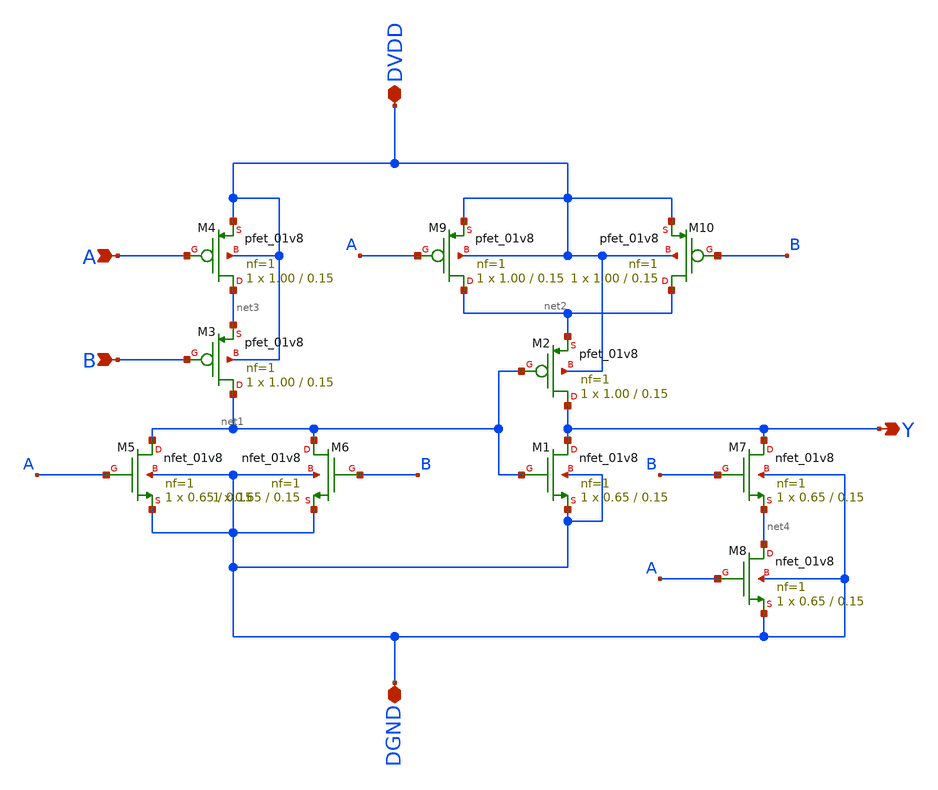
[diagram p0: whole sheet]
** sch_path: project/sch_sym_files/xor2.sch
**.subckt xor2 DVDD DGND A B Y
*.iopin DVDD
*.iopin DGND
*.ipin A
*.ipin B
*.opin Y
XM2 Y net1 net2 DVDD sky130_fd_pr__pfet_01v8 L=0.15 W=1.00 nf=1 ad='int((nf+1)/2) * W/nf * 0.29' as='int((nf+2)/2) * W/nf * 0.29'
+ pd='2*int((nf+1)/2) * (W/nf + 0.29)' ps='2*int((nf+2)/2) * (W/nf + 0.29)' nrd='0.29 / W' nrs='0.29 / W'
+ sa=0 sb=0 sd=0 mult=1 m=1
XM1 Y net1 DGND DGND sky130_fd_pr__nfet_01v8 L=0.15 W=0.65 nf=1 ad='int((nf+1)/2) * W/nf * 0.29' as='int((nf+2)/2) * W/nf * 0.29'
+ pd='2*int((nf+1)/2) * (W/nf + 0.29)' ps='2*int((nf+2)/2) * (W/nf + 0.29)' nrd='0.29 / W' nrs='0.29 / W'
+ sa=0 sb=0 sd=0 mult=1 m=1
XM3 net1 B net3 DVDD sky130_fd_pr__pfet_01v8 L=0.15 W=1.00 nf=1 ad='int((nf+1)/2) * W/nf * 0.29' as='int((nf+2)/2) * W/nf * 0.29'
+ pd='2*int((nf+1)/2) * (W/nf + 0.29)' ps='2*int((nf+2)/2) * (W/nf + 0.29)' nrd='0.29 / W' nrs='0.29 / W'
+ sa=0 sb=0 sd=0 mult=1 m=1
XM4 net3 A DVDD DVDD sky130_fd_pr__pfet_01v8 L=0.15 W=1.00 nf=1 ad='int((nf+1)/2) * W/nf * 0.29' as='int((nf+2)/2) * W/nf * 0.29'
+ pd='2*int((nf+1)/2) * (W/nf + 0.29)' ps='2*int((nf+2)/2) * (W/nf + 0.29)' nrd='0.29 / W' nrs='0.29 / W'
+ sa=0 sb=0 sd=0 mult=1 m=1
XM5 net1 A DGND DGND sky130_fd_pr__nfet_01v8 L=0.15 W=0.65 nf=1 ad='int((nf+1)/2) * W/nf * 0.29' as='int((nf+2)/2) * W/nf * 0.29'
+ pd='2*int((nf+1)/2) * (W/nf + 0.29)' ps='2*int((nf+2)/2) * (W/nf + 0.29)' nrd='0.29 / W' nrs='0.29 / W'
+ sa=0 sb=0 sd=0 mult=1 m=1
XM6 net1 B DGND DGND sky130_fd_pr__nfet_01v8 L=0.15 W=0.65 nf=1 ad='int((nf+1)/2) * W/nf * 0.29' as='int((nf+2)/2) * W/nf * 0.29'
+ pd='2*int((nf+1)/2) * (W/nf + 0.29)' ps='2*int((nf+2)/2) * (W/nf + 0.29)' nrd='0.29 / W' nrs='0.29 / W'
+ sa=0 sb=0 sd=0 mult=1 m=1
XM7 Y B net4 DGND sky130_fd_pr__nfet_01v8 L=0.15 W=0.65 nf=1 ad='int((nf+1)/2) * W/nf * 0.29' as='int((nf+2)/2) * W/nf * 0.29'
+ pd='2*int((nf+1)/2) * (W/nf + 0.29)' ps='2*int((nf+2)/2) * (W/nf + 0.29)' nrd='0.29 / W' nrs='0.29 / W'
+ sa=0 sb=0 sd=0 mult=1 m=1
XM8 net4 A DGND DGND sky130_fd_pr__nfet_01v8 L=0.15 W=0.65 nf=1 ad='int((nf+1)/2) * W/nf * 0.29' as='int((nf+2)/2) * W/nf * 0.29'
+ pd='2*int((nf+1)/2) * (W/nf + 0.29)' ps='2*int((nf+2)/2) * (W/nf + 0.29)' nrd='0.29 / W' nrs='0.29 / W'
+ sa=0 sb=0 sd=0 mult=1 m=1
XM9 net2 A DVDD DVDD sky130_fd_pr__pfet_01v8 L=0.15 W=1.00 nf=1 ad='int((nf+1)/2) * W/nf * 0.29' as='int((nf+2)/2) * W/nf * 0.29'
+ pd='2*int((nf+1)/2) * (W/nf + 0.29)' ps='2*int((nf+2)/2) * (W/nf + 0.29)' nrd='0.29 / W' nrs='0.29 / W'
+ sa=0 sb=0 sd=0 mult=1 m=1
XM10 net2 B DVDD DVDD sky130_fd_pr__pfet_01v8 L=0.15 W=1.00 nf=1 ad='int((nf+1)/2) * W/nf * 0.29' as='int((nf+2)/2) * W/nf * 0.29'
+ pd='2*int((nf+1)/2) * (W/nf + 0.29)' ps='2*int((nf+2)/2) * (W/nf + 0.29)' nrd='0.29 / W' nrs='0.29 / W'
+ sa=0 sb=0 sd=0 mult=1 m=1
**.ends
.end
